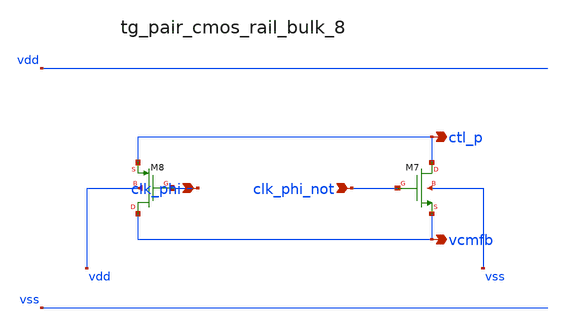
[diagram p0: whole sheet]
** sch_path: analog-db/raw/cmfb_004_output_switched_cap/hier/blocks/tg_pair_cmos_rail_bulk_8.sch
**.subckt tg_pair_cmos_rail_bulk_8 clk_phi clk_phi_not ctl_p vcmfb
*.ipin clk_phi
*.ipin clk_phi_not
*.opin ctl_p
*.opin vcmfb
XM7 ctl_p clk_phi_not vcmfb vss sg13_lv_nmos w=x_dut_xm7_w l=x_dut_xm7_l ng=1 m=x_dut_xm7_m
XM8 vcmfb clk_phi ctl_p vdd sg13_lv_pmos w=x_dut_xm8_w l=x_dut_xm8_l ng=1 m=x_dut_xm8_m
**.ends
.end
